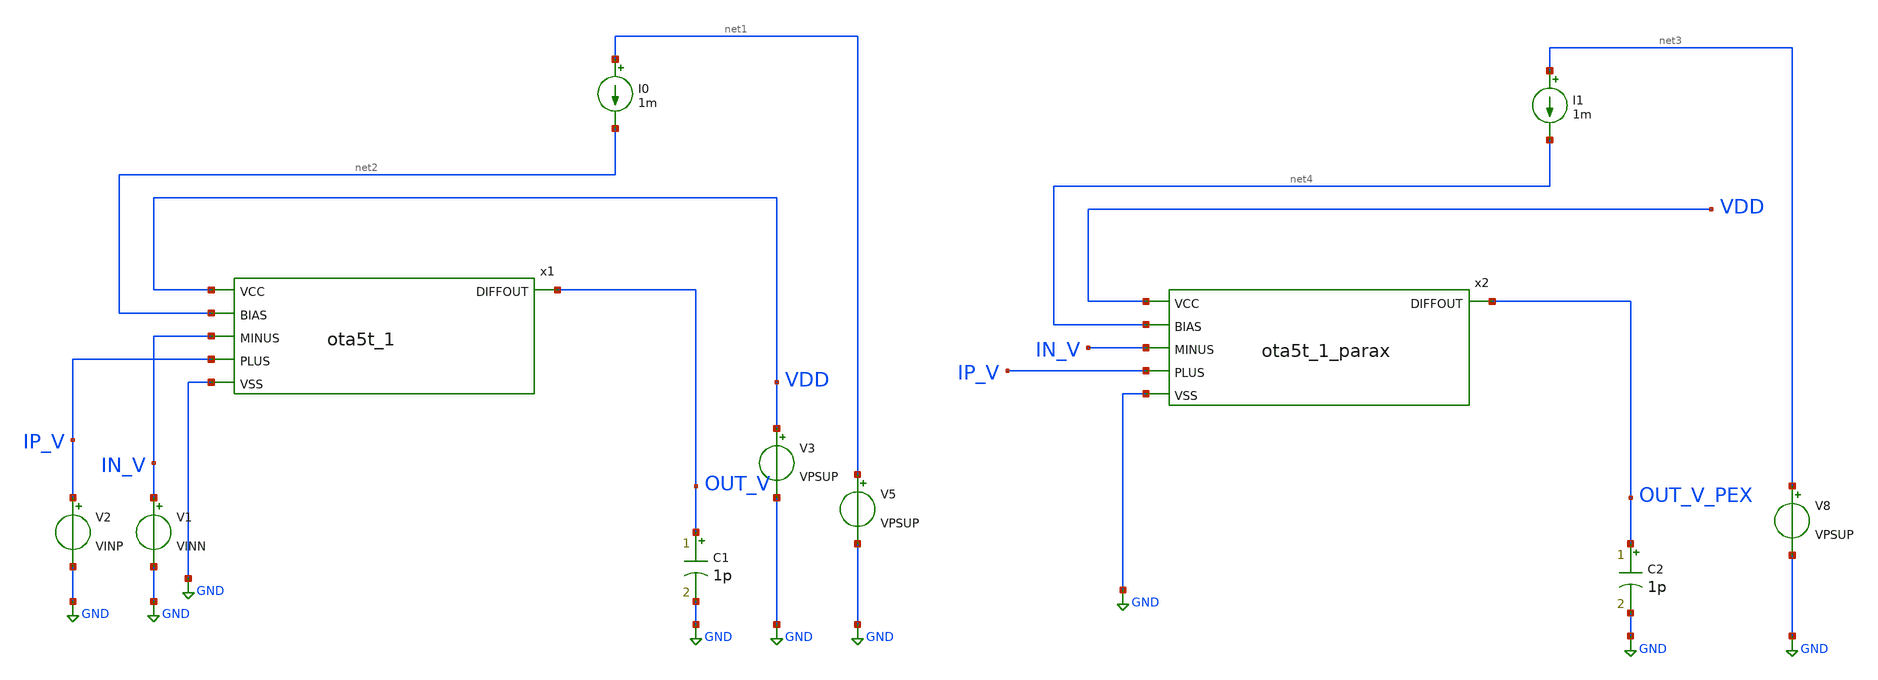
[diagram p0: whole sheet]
** sch_path: xschem/ota5t_1__TB_PEX.sch
**.subckt ota5t_1__TB_PEX
C1 OUT_V GND 1p m=1
V1 IN_V GND VINN
V2 IP_V GND VINP
V3 VDD GND VPSUP
I0 net1 net2 1m
V5 net1 GND VPSUP
x1 VDD OUT_V net2 IN_V IP_V GND ota5t_1
C2 OUT_V_PEX GND 1p m=1
I1 net3 net4 1m
V8 net3 GND VPSUP
x2 VDD OUT_V_PEX net4 IN_V IP_V GND ota5t_1_parax
**** begin user architecture code



* ngspice commands
.options savecurrents
*vPSUP PSUP 0 1.8
*vBULK PBULK 0 1.8
*vNSUP NSUP 0 0
*vNBULK NBULK 0 0
*vINP INP 0 0.45
*vINN INN 0 0.45
*iIBIAS IBIAS 0 1e-3
.param VPSUP =1.8   VINN = 1.0  VINP = 0.9
.control
  save all
  shell rm -f ota5t_1_delete_typ.raw
  set appendwrite
  dc V2 0 1.8 0.001
  remzerovec
  write ota5t_1_delete_typ.raw
.endc



.lib $::SKYWATER_MODELS/sky130.lib.spice tt
**** end user architecture code
**.ends

* expanding   symbol:  ota5t_1.sym # of pins=6
** sym_path: xschem/ota5t_1.sym
** sch_path: xschem/ota5t_1.sch
.subckt ota5t_1 VCC DIFFOUT BIAS MINUS PLUS VSS
*.ipin PLUS
*.ipin MINUS
*.ipin VCC
*.ipin VSS
*.ipin BIAS
*.opin DIFFOUT
XM7 DIFFOUT Vleft VCC VCC sky130_fd_pr__pfet_01v8_lvt L=2 W=5 nf=1 ad='int((nf+1)/2) * W/nf * 0.29' as='int((nf+2)/2) * W/nf * 0.29'
+ pd='2*int((nf+1)/2) * (W/nf + 0.29)' ps='2*int((nf+2)/2) * (W/nf + 0.29)' nrd='0.29 / W' nrs='0.29 / W'
+ sa=0 sb=0 sd=0 mult=1 m=1
XM2 Vleft Vleft VCC VCC sky130_fd_pr__pfet_01v8_lvt L=2 W=5 nf=1 ad='int((nf+1)/2) * W/nf * 0.29' as='int((nf+2)/2) * W/nf * 0.29'
+ pd='2*int((nf+1)/2) * (W/nf + 0.29)' ps='2*int((nf+2)/2) * (W/nf + 0.29)' nrd='0.29 / W' nrs='0.29 / W'
+ sa=0 sb=0 sd=0 mult=1 m=1
XM6 Vleft PLUS net1 VSS sky130_fd_pr__nfet_01v8_lvt L=0.5 W=2 nf=1 ad='int((nf+1)/2) * W/nf * 0.29' as='int((nf+2)/2) * W/nf * 0.29'
+ pd='2*int((nf+1)/2) * (W/nf + 0.29)' ps='2*int((nf+2)/2) * (W/nf + 0.29)' nrd='0.29 / W' nrs='0.29 / W'
+ sa=0 sb=0 sd=0 mult=1 m=1
XM4 DIFFOUT MINUS net1 VSS sky130_fd_pr__nfet_01v8_lvt L=0.5 W=2 nf=1 ad='int((nf+1)/2) * W/nf * 0.29'
+ as='int((nf+2)/2) * W/nf * 0.29' pd='2*int((nf+1)/2) * (W/nf + 0.29)' ps='2*int((nf+2)/2) * (W/nf + 0.29)'
+ nrd='0.29 / W' nrs='0.29 / W' sa=0 sb=0 sd=0 mult=1 m=1
XM1 net1 BIAS VSS VSS sky130_fd_pr__nfet_01v8 L=2 W=4 nf=1 ad='int((nf+1)/2) * W/nf * 0.29' as='int((nf+2)/2) * W/nf * 0.29'
+ pd='2*int((nf+1)/2) * (W/nf + 0.29)' ps='2*int((nf+2)/2) * (W/nf + 0.29)' nrd='0.29 / W' nrs='0.29 / W'
+ sa=0 sb=0 sd=0 mult=1 m=1
XM3 BIAS BIAS VSS VSS sky130_fd_pr__nfet_01v8 L=2 W=4 nf=1 ad='int((nf+1)/2) * W/nf * 0.29' as='int((nf+2)/2) * W/nf * 0.29'
+ pd='2*int((nf+1)/2) * (W/nf + 0.29)' ps='2*int((nf+2)/2) * (W/nf + 0.29)' nrd='0.29 / W' nrs='0.29 / W'
+ sa=0 sb=0 sd=0 mult=1 m=1
XC1 DIFFOUT VSS sky130_fd_pr__cap_mim_m3_1 W=10 L=10 MF=10 m=10
.ends


* expanding   symbol:  ota5t_1_parax.sym # of pins=6
** sym_path: xschem/ota5t_1.sym
.include [file normalize ../mag/ota5t_1.sim.spice]
.GLOBAL GND
.end
